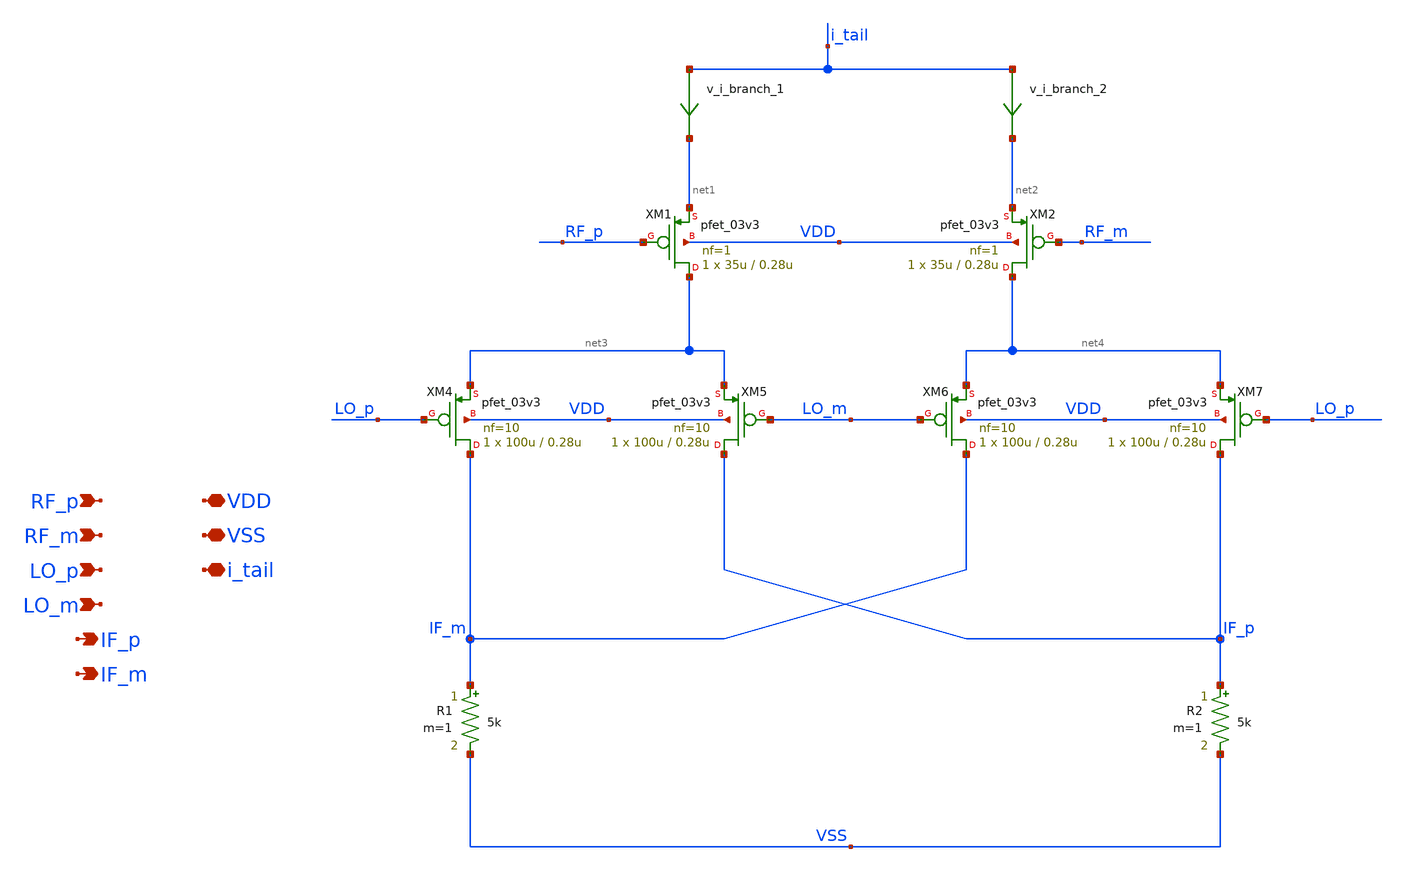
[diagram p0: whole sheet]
** sch_path: designs/mixer/schematic/Lei_mixer.sch
**.subckt Lei_mixer VDD VSS RF_p RF_m LO_p LO_m IF_p IF_m i_tail
*.iopin VDD
*.iopin VSS
*.ipin RF_p
*.ipin RF_m
*.ipin LO_p
*.ipin LO_m
*.opin IF_p
*.opin IF_m
*.iopin i_tail
XM1 net3 RF_p net1 VDD pfet_03v3 L=0.28u W=35u nf=1 ad='int((nf+1)/2) * W/nf * 0.18u' as='int((nf+2)/2) * W/nf * 0.18u'
+ pd='2*int((nf+1)/2) * (W/nf + 0.18u)' ps='2*int((nf+2)/2) * (W/nf + 0.18u)' nrd='0.18u / W' nrs='0.18u / W'
+ sa=0 sb=0 sd=0 m=1
XM2 net4 RF_m net2 VDD pfet_03v3 L=0.28u W=35u nf=1 ad='int((nf+1)/2) * W/nf * 0.18u' as='int((nf+2)/2) * W/nf * 0.18u'
+ pd='2*int((nf+1)/2) * (W/nf + 0.18u)' ps='2*int((nf+2)/2) * (W/nf + 0.18u)' nrd='0.18u / W' nrs='0.18u / W'
+ sa=0 sb=0 sd=0 m=1
XM4 IF_m LO_p net3 VDD pfet_03v3 L=0.28u W=100u nf=10 ad='int((nf+1)/2) * W/nf * 0.18u' as='int((nf+2)/2) * W/nf * 0.18u'
+ pd='2*int((nf+1)/2) * (W/nf + 0.18u)' ps='2*int((nf+2)/2) * (W/nf + 0.18u)' nrd='0.18u / W' nrs='0.18u / W'
+ sa=0 sb=0 sd=0 m=1
XM5 IF_p LO_m net3 VDD pfet_03v3 L=0.28u W=100u nf=10 ad='int((nf+1)/2) * W/nf * 0.18u' as='int((nf+2)/2) * W/nf * 0.18u'
+ pd='2*int((nf+1)/2) * (W/nf + 0.18u)' ps='2*int((nf+2)/2) * (W/nf + 0.18u)' nrd='0.18u / W' nrs='0.18u / W'
+ sa=0 sb=0 sd=0 m=1
XM6 IF_m LO_m net4 VDD pfet_03v3 L=0.28u W=100u nf=10 ad='int((nf+1)/2) * W/nf * 0.18u' as='int((nf+2)/2) * W/nf * 0.18u'
+ pd='2*int((nf+1)/2) * (W/nf + 0.18u)' ps='2*int((nf+2)/2) * (W/nf + 0.18u)' nrd='0.18u / W' nrs='0.18u / W'
+ sa=0 sb=0 sd=0 m=1
XM7 IF_p LO_p net4 VDD pfet_03v3 L=0.28u W=100u nf=10 ad='int((nf+1)/2) * W/nf * 0.18u' as='int((nf+2)/2) * W/nf * 0.18u'
+ pd='2*int((nf+1)/2) * (W/nf + 0.18u)' ps='2*int((nf+2)/2) * (W/nf + 0.18u)' nrd='0.18u / W' nrs='0.18u / W'
+ sa=0 sb=0 sd=0 m=1
R1 IF_m VSS 5k m=1
R2 IF_p VSS 5k m=1
v_i_branch_1 i_tail net1 0
.save i(v_i_branch_1)
v_i_branch_2 i_tail net2 0
.save i(v_i_branch_2)
**.ends
.end
